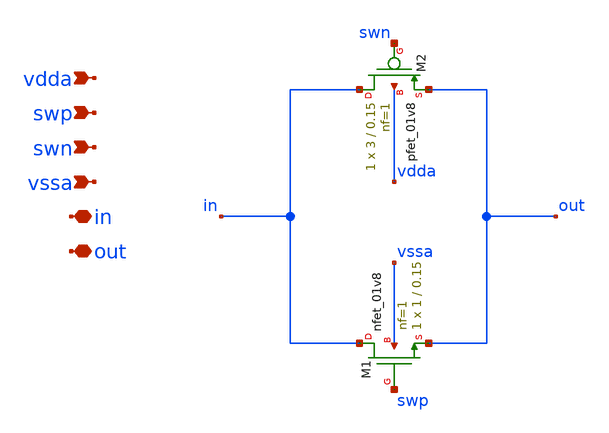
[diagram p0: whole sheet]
** sch_path: xschem/schematics/tg_sw.sch
**.subckt tg_sw vdda swp swn vssa in out
*.ipin vdda
*.ipin swp
*.ipin swn
*.ipin vssa
*.iopin in
*.iopin out
XM1 in swp out vssa sky130_fd_pr__nfet_01v8 L=0.15 W=1 nf=1 ad='int((nf+1)/2) * W/nf * 0.29' as='int((nf+2)/2) * W/nf * 0.29'
+ pd='2*int((nf+1)/2) * (W/nf + 0.29)' ps='2*int((nf+2)/2) * (W/nf + 0.29)' nrd='0.29 / W' nrs='0.29 / W'
+ sa=0 sb=0 sd=0 mult=1 m=1
XM2 in swn out vdda sky130_fd_pr__pfet_01v8 L=0.15 W=3 nf=1 ad='int((nf+1)/2) * W/nf * 0.29' as='int((nf+2)/2) * W/nf * 0.29'
+ pd='2*int((nf+1)/2) * (W/nf + 0.29)' ps='2*int((nf+2)/2) * (W/nf + 0.29)' nrd='0.29 / W' nrs='0.29 / W'
+ sa=0 sb=0 sd=0 mult=1 m=1
**.ends
.end
